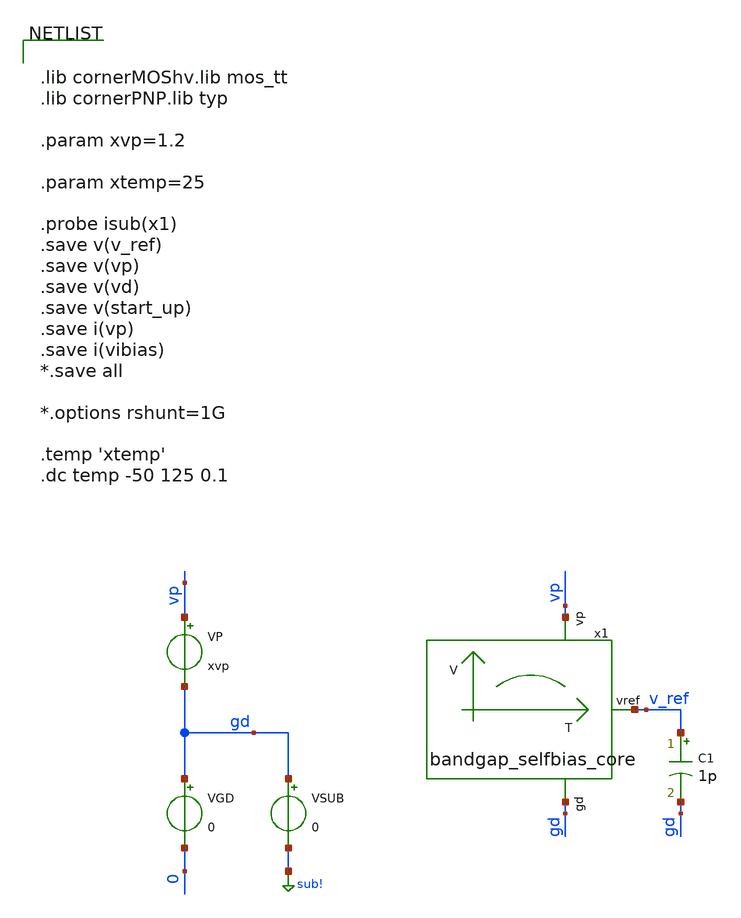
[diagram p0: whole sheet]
** sch_path: testbench/bandgap_selfbias_core_temp_sweep_tb.sch
**.subckt bandgap_selfbias_core_temp_sweep_tb
VGD gd 0 0
VP vp gd xvp
.save i(vp)
VSUB gd sub! 0
C1 v_ref gd 1p m=1
x1 vp v_ref gd bandgap_selfbias_core
**** begin user architecture code


.lib cornerMOShv.lib mos_tt
.lib cornerPNP.lib typ

.param xvp=1.2

.param xtemp=25

.probe isub(x1)
.save v(v_ref)
.save v(vp)
.save v(vd)
.save v(start_up)
.save i(vp)
.save i(vibias)
*.save all

*.options rshunt=1G

.temp 'xtemp'
.dc temp -50 125 0.1


**** end user architecture code
**.ends

* expanding   symbol:  /foss/designs/test/circuit/bandgap_selfbias_core.sym # of pins=3
** sym_path: /foss/designs/test/circuit/bandgap_selfbias_core.sym
** sch_path: /foss/designs/test/circuit/bandgap_selfbias_core.sch
.subckt bandgap_selfbias_core vp vref gd
*.ipin gd
*.ipin vp
*.opin vref
XM1 net1 net1 gd gd sg13_hv_nmos w=1.2u l=0.9u ng=1 m=2 mm_ok=1
XM2 net4 net1 net5 gd sg13_hv_nmos w=1.2u l=0.9u ng=1 m=8 mm_ok=1
XM7 net5 vref gd gd sg13_hv_nmos w=1.2u l=0.9u ng=1 m=4 mm_ok=1
XM3 net2 net2 net1 gd sg13_hv_nmos w=1.2u l=0.9u ng=1 m=2 mm_ok=1
XM4 net3 net2 net4 gd sg13_hv_nmos w=1.2u l=0.9u ng=1 m=8 mm_ok=1
XM6 net3 net3 vp vp sg13_hv_pmos w=1.2u l=0.9u ng=1 m=2 mm_ok=1
XM5 net2 net3 vp vp sg13_hv_pmos w=1.2u l=0.9u ng=1 m=2 mm_ok=1
XM10 net6 net3 vp vp sg13_hv_pmos w=1.2u l=0.9u ng=1 m=2 mm_ok=1
XM8 net7 net6 gd gd sg13_hv_nmos w=1.2u l=0.9u ng=1 m=20 mm_ok=1
XM9 net6 net6 net7 gd sg13_hv_nmos w=1.2u l=0.9u ng=1 m=12 mm_ok=1
XM13 net8 net3 vp vp sg13_hv_pmos w=1.2u l=0.9u ng=1 m=2 mm_ok=1
XM11 net9 net8 net7 gd sg13_hv_nmos w=1.2u l=0.9u ng=1 m=20 mm_ok=1
XM12 net8 net8 net9 gd sg13_hv_nmos w=1.2u l=0.9u ng=1 m=10 mm_ok=1
XM14 vref vref net9 gd sg13_hv_nmos w=1.2u l=0.9u ng=1 m=8 mm_ok=1
XM15 vref net3 vp vp sg13_hv_pmos w=1.2u l=0.9u ng=1 m=2 mm_ok=1
.ends

.GLOBAL sub!
.end
